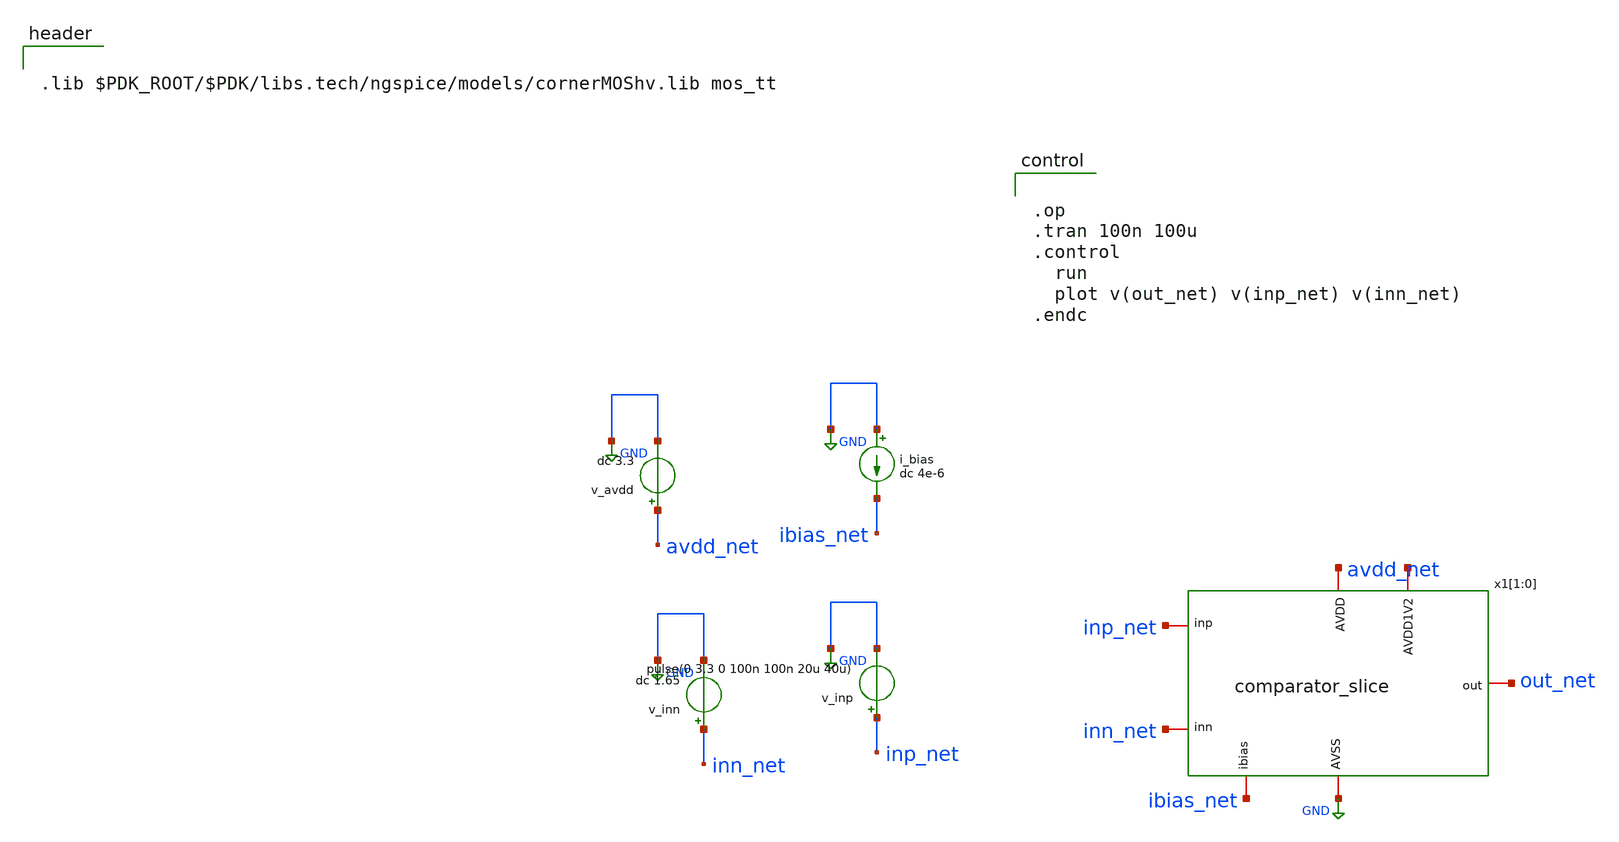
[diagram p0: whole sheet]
** sch_path: macros/comparator/testbenches/xschem/tb_comparator_slice.sch
**.subckt tb_comparator_slice
v_avdd avdd_net GND dc 3.3
v_inn inn_net GND dc 1.65
v_inp inp_net GND pulse(0 3.3 0 100n 100n 20u 40u)
i_bias GND ibias_net dc 4e-6
x1[1] inp_net inn_net ibias_net out_net avdd_net GND net1[1] comparator_slice
x1[0] inp_net inn_net ibias_net out_net avdd_net GND net1[0] comparator_slice
**** begin user architecture code


.lib $PDK_ROOT/$PDK/libs.tech/ngspice/models/cornerMOShv.lib mos_tt




.op
.tran 100n 100u
.control
  run
  plot v(out_net) v(inp_net) v(inn_net)
.endc


**** end user architecture code
**.ends
.GLOBAL GND
.end
